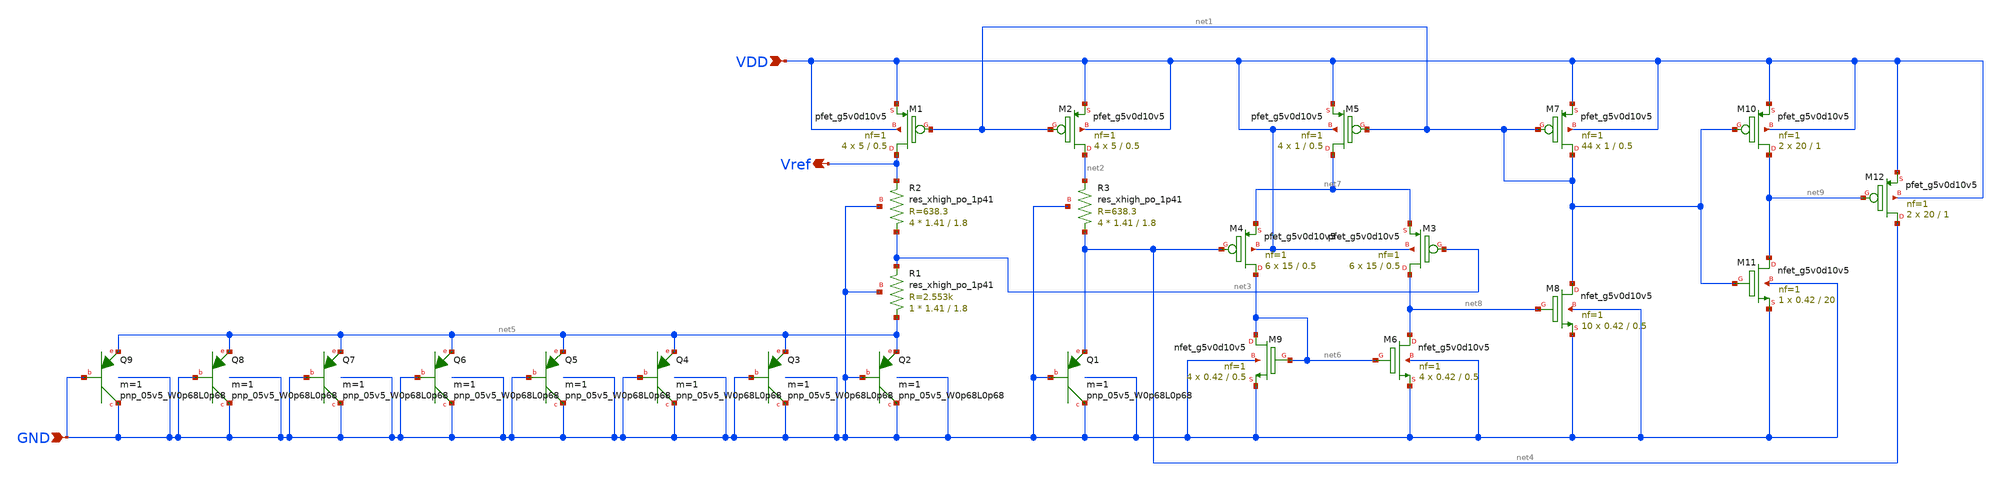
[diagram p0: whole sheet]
** sch_path: Analog_Blocks/Bandgap/Schematics/BGR1.8v_2/Bandgap_2.sch
**.subckt Bandgap_2 VDD GND Vref
*.ipin VDD
*.ipin GND
*.opin Vref
XM1 Vref net1 VDD VDD sky130_fd_pr__pfet_g5v0d10v5 L=0.5 W=5 nf=1 ad='int((nf+1)/2) * W/nf * 0.29' as='int((nf+2)/2) * W/nf * 0.29'
+ pd='2*int((nf+1)/2) * (W/nf + 0.29)' ps='2*int((nf+2)/2) * (W/nf + 0.29)' nrd='0.29 / W' nrs='0.29 / W'
+ sa=0 sb=0 sd=0 mult=4 m=4
XM2 net2 net1 VDD VDD sky130_fd_pr__pfet_g5v0d10v5 L=0.5 W=5 nf=1 ad='int((nf+1)/2) * W/nf * 0.29' as='int((nf+2)/2) * W/nf * 0.29'
+ pd='2*int((nf+1)/2) * (W/nf + 0.29)' ps='2*int((nf+2)/2) * (W/nf + 0.29)' nrd='0.29 / W' nrs='0.29 / W'
+ sa=0 sb=0 sd=0 mult=4 m=4
XQ1 GND GND net4 sky130_fd_pr__pnp_05v5_W0p68L0p68 m=1
XQ2 GND GND net5 sky130_fd_pr__pnp_05v5_W0p68L0p68 m=1
XQ3 GND GND net5 sky130_fd_pr__pnp_05v5_W0p68L0p68 m=1
XQ4 GND GND net5 sky130_fd_pr__pnp_05v5_W0p68L0p68 m=1
XQ5 GND GND net5 sky130_fd_pr__pnp_05v5_W0p68L0p68 m=1
XQ6 GND GND net5 sky130_fd_pr__pnp_05v5_W0p68L0p68 m=1
XQ7 GND GND net5 sky130_fd_pr__pnp_05v5_W0p68L0p68 m=1
XQ8 GND GND net5 sky130_fd_pr__pnp_05v5_W0p68L0p68 m=1
XQ9 GND GND net5 sky130_fd_pr__pnp_05v5_W0p68L0p68 m=1
XR1 net5 net3 GND sky130_fd_pr__res_xhigh_po_1p41 L=1.8 mult=1 m=1
XR2 net3 Vref GND sky130_fd_pr__res_xhigh_po_1p41 L=1.8 mult=4 m=4
XR3 net4 net2 GND sky130_fd_pr__res_xhigh_po_1p41 L=1.8 mult=4 m=4
XM5 net7 net1 VDD VDD sky130_fd_pr__pfet_g5v0d10v5 L=0.5 W=1 nf=1 ad='int((nf+1)/2) * W/nf * 0.29' as='int((nf+2)/2) * W/nf * 0.29'
+ pd='2*int((nf+1)/2) * (W/nf + 0.29)' ps='2*int((nf+2)/2) * (W/nf + 0.29)' nrd='0.29 / W' nrs='0.29 / W'
+ sa=0 sb=0 sd=0 mult=4 m=4
XM7 net1 net1 VDD VDD sky130_fd_pr__pfet_g5v0d10v5 L=0.5 W=1 nf=1 ad='int((nf+1)/2) * W/nf * 0.29' as='int((nf+2)/2) * W/nf * 0.29'
+ pd='2*int((nf+1)/2) * (W/nf + 0.29)' ps='2*int((nf+2)/2) * (W/nf + 0.29)' nrd='0.29 / W' nrs='0.29 / W'
+ sa=0 sb=0 sd=0 mult=44 m=44
XM3 net8 net3 net7 VDD sky130_fd_pr__pfet_g5v0d10v5 L=0.5 W=15 nf=1 ad='int((nf+1)/2) * W/nf * 0.29'
+ as='int((nf+2)/2) * W/nf * 0.29' pd='2*int((nf+1)/2) * (W/nf + 0.29)' ps='2*int((nf+2)/2) * (W/nf + 0.29)'
+ nrd='0.29 / W' nrs='0.29 / W' sa=0 sb=0 sd=0 mult=6 m=6
XM4 net6 net4 net7 VDD sky130_fd_pr__pfet_g5v0d10v5 L=0.5 W=15 nf=1 ad='int((nf+1)/2) * W/nf * 0.29'
+ as='int((nf+2)/2) * W/nf * 0.29' pd='2*int((nf+1)/2) * (W/nf + 0.29)' ps='2*int((nf+2)/2) * (W/nf + 0.29)'
+ nrd='0.29 / W' nrs='0.29 / W' sa=0 sb=0 sd=0 mult=6 m=6
XM8 net1 net8 GND GND sky130_fd_pr__nfet_g5v0d10v5 L=0.5 W=0.42 nf=1 ad='int((nf+1)/2) * W/nf * 0.29'
+ as='int((nf+2)/2) * W/nf * 0.29' pd='2*int((nf+1)/2) * (W/nf + 0.29)' ps='2*int((nf+2)/2) * (W/nf + 0.29)'
+ nrd='0.29 / W' nrs='0.29 / W' sa=0 sb=0 sd=0 mult=10 m=10
XM6 net8 net6 GND GND sky130_fd_pr__nfet_g5v0d10v5 L=0.5 W=0.42 nf=1 ad='int((nf+1)/2) * W/nf * 0.29'
+ as='int((nf+2)/2) * W/nf * 0.29' pd='2*int((nf+1)/2) * (W/nf + 0.29)' ps='2*int((nf+2)/2) * (W/nf + 0.29)'
+ nrd='0.29 / W' nrs='0.29 / W' sa=0 sb=0 sd=0 mult=4 m=4
XM9 net6 net6 GND GND sky130_fd_pr__nfet_g5v0d10v5 L=0.5 W=0.42 nf=1 ad='int((nf+1)/2) * W/nf * 0.29'
+ as='int((nf+2)/2) * W/nf * 0.29' pd='2*int((nf+1)/2) * (W/nf + 0.29)' ps='2*int((nf+2)/2) * (W/nf + 0.29)'
+ nrd='0.29 / W' nrs='0.29 / W' sa=0 sb=0 sd=0 mult=4 m=4
XM10 net9 net1 VDD VDD sky130_fd_pr__pfet_g5v0d10v5 L=1 W=20 nf=1 ad='int((nf+1)/2) * W/nf * 0.29' as='int((nf+2)/2) * W/nf * 0.29'
+ pd='2*int((nf+1)/2) * (W/nf + 0.29)' ps='2*int((nf+2)/2) * (W/nf + 0.29)' nrd='0.29 / W' nrs='0.29 / W'
+ sa=0 sb=0 sd=0 mult=2 m=2
XM11 net9 net1 GND GND sky130_fd_pr__nfet_g5v0d10v5 L=20 W=0.42 nf=1 ad='int((nf+1)/2) * W/nf * 0.29'
+ as='int((nf+2)/2) * W/nf * 0.29' pd='2*int((nf+1)/2) * (W/nf + 0.29)' ps='2*int((nf+2)/2) * (W/nf + 0.29)'
+ nrd='0.29 / W' nrs='0.29 / W' sa=0 sb=0 sd=0 mult=1 m=1
XM12 net4 net9 VDD VDD sky130_fd_pr__pfet_g5v0d10v5 L=1 W=20 nf=1 ad='int((nf+1)/2) * W/nf * 0.29' as='int((nf+2)/2) * W/nf * 0.29'
+ pd='2*int((nf+1)/2) * (W/nf + 0.29)' ps='2*int((nf+2)/2) * (W/nf + 0.29)' nrd='0.29 / W' nrs='0.29 / W'
+ sa=0 sb=0 sd=0 mult=2 m=2
**.ends
.end
